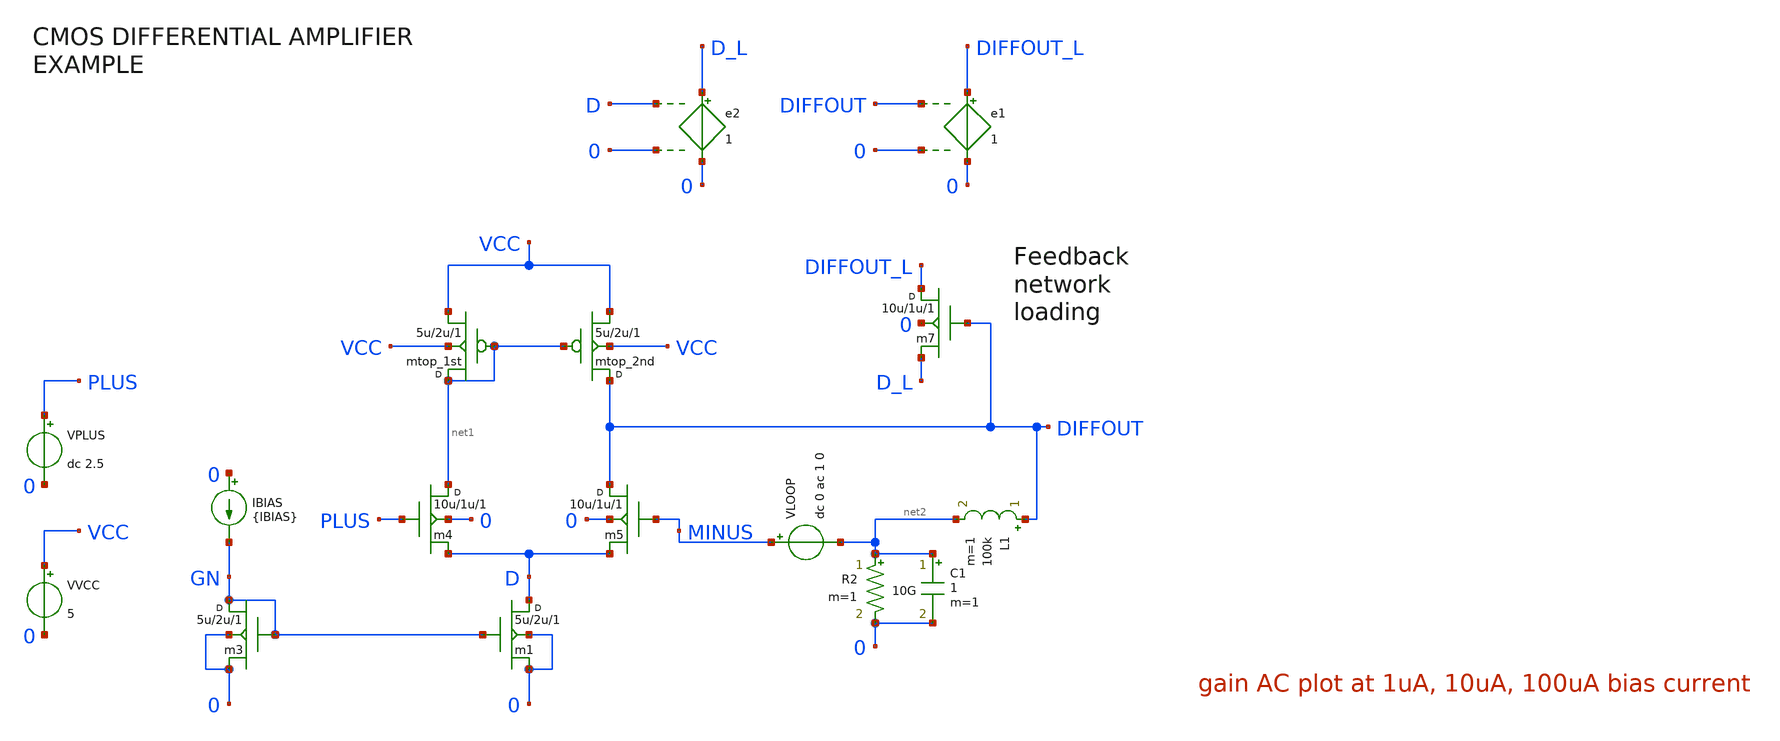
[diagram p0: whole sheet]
** sch_path: xschem_library/examples/test_ac.sch
* Copyright (C) 1998-2026 Stefan Frederik Schippers
* This program is free software; you can redistribute it and/or modify
* it under the terms of the GNU General Public License as published by
* the Free Software Foundation; either version 2 of the License, or
* (at your option) any later version.
* This program is distributed in the hope that it will be useful,
* but WITHOUT ANY WARRANTY; without even the implied warranty of
* MERCHANTABILITY or FITNESS FOR A PARTICULAR PURPOSE.  See the
* GNU General Public License for more details.
* You should have received a copy of the GNU General Public License
* along with this program; if not, write to the Free Software
**.subckt test_ac
m1 D GN 0 0 cmosn w=5u l=2u m=1
mtop_2nd DIFFOUT net1 VCC VCC cmosp w=5u l=2u m=1
VVCC VCC 0 5
m3 GN GN 0 0 cmosn w=5u l=2u m=1
IBIAS 0 GN {IBIAS}
m4 net1 PLUS D 0 cmosn w=10u l=1u m=1
m5 DIFFOUT MINUS D 0 cmosn w=10u l=1u m=1
mtop_1st net1 net1 VCC VCC cmosp w=5u l=2u m=1
VPLUS PLUS 0 dc 2.5
e1 DIFFOUT_L 0 DIFFOUT 0 1
e2 D_L 0 D 0 1
m7 DIFFOUT_L DIFFOUT D_L 0 cmosn w=10u l=1u m=1
VLOOP MINUS net2 dc 0 ac 1 0
R2 net2 0 10G m=1
L1 DIFFOUT net2 100k m=1
C1 net2 0 1 m=1
**** begin user architecture code


.temp 30

** models are generally not free: you must download
** SPICE models for active devices and put them  into the below
** referenced file in netlist/simulation directory.
** http://bwrcs.eecs.berkeley.edu/Classes/icdesign/ee241_s00/ASSIGNMENTS/TSMC035-n96g-params.txt
.options savecurrents
.include "models_cmos_example.txt"

.param IBIAS=1u
.control
save all
op
write test_ac.raw
set appendwrite

ac dec 10 1000 10G
remzerovec
write test_ac.raw
alter IBIAS=10u
ac dec 10 1000 10G
remzerovec
write test_ac.raw
alter IBIAS=100u
ac dec 10 1000 10G
remzerovec
write test_ac.raw

.endc






**** end user architecture code
**.ends
.end
